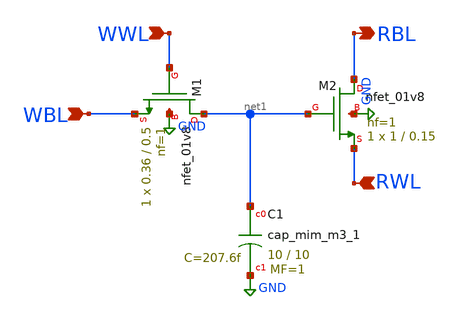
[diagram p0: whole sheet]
** sch_path: analog/schematics/Core/BitCell_2T1C.sch
**.subckt BitCell_2T1C WBL RWL WWL RBL
*.ipin WBL
*.ipin RWL
*.ipin WWL
*.opin RBL
XM1 net1 WWL WBL GND sky130_fd_pr__nfet_01v8 L=0.5 W=0.36 nf=1 ad='int((nf+1)/2) * W/nf * 0.29' as='int((nf+2)/2) * W/nf * 0.29'
+ pd='2*int((nf+1)/2) * (W/nf + 0.29)' ps='2*int((nf+2)/2) * (W/nf + 0.29)' nrd='0.29 / W' nrs='0.29 / W'
+ sa=0 sb=0 sd=0 mult=1 m=1
XM2 RBL net1 RWL GND sky130_fd_pr__nfet_01v8 L=0.15 W=1 nf=1 ad='int((nf+1)/2) * W/nf * 0.29' as='int((nf+2)/2) * W/nf * 0.29'
+ pd='2*int((nf+1)/2) * (W/nf + 0.29)' ps='2*int((nf+2)/2) * (W/nf + 0.29)' nrd='0.29 / W' nrs='0.29 / W'
+ sa=0 sb=0 sd=0 mult=1 m=1
XC1 net1 GND sky130_fd_pr__cap_mim_m3_1 W=10 L=10 MF=1 m=1
**.ends
.GLOBAL GND
.end
